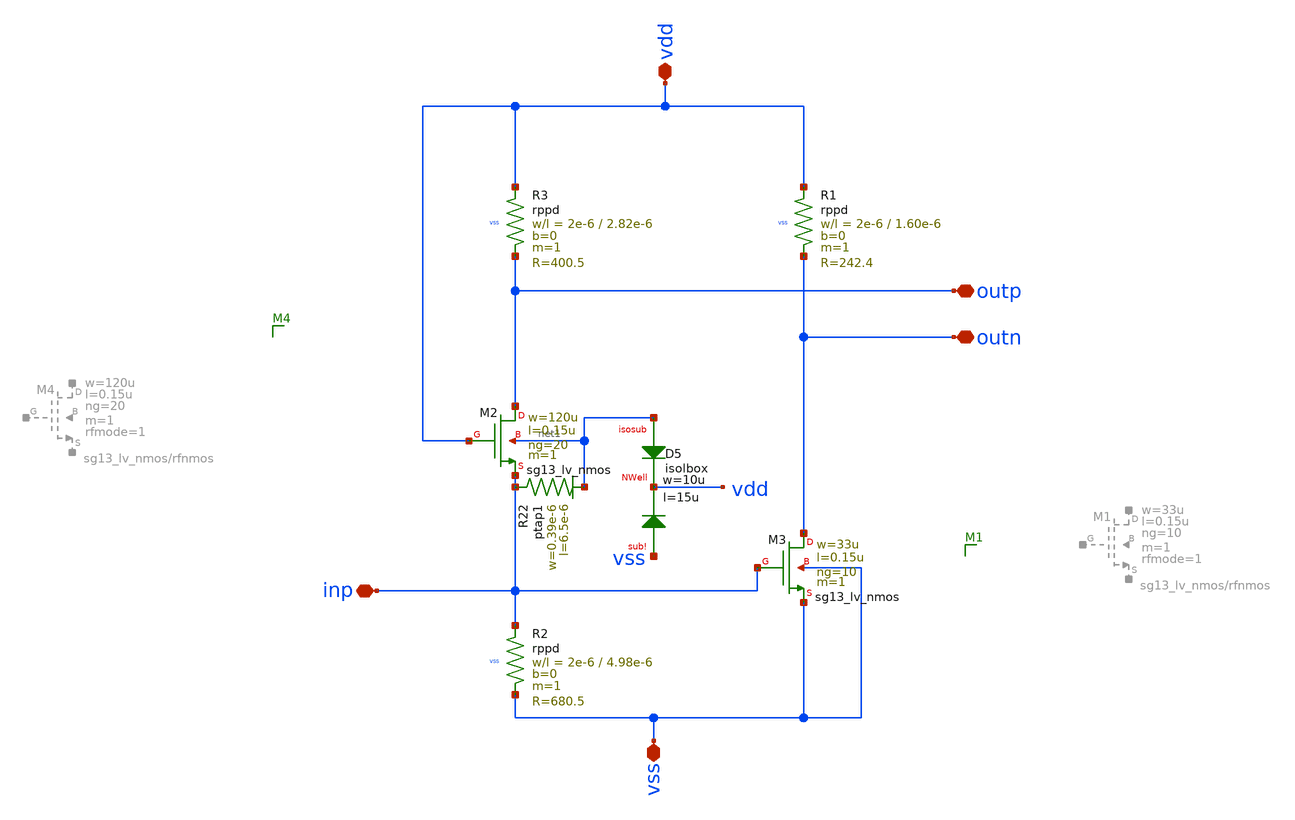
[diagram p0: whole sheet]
** sch_path: LNA7096-main/schematic/xschem/02_s2d/s2d.sch
**.subckt s2d vdd vss outp outn inp
*.iopin vdd
*.iopin vss
*.iopin outp
*.iopin outn
*.iopin inp
XR3 vdd outp vss rppd w=2e-6 l=2.82e-6 m=1 b=0 mm_ok=1
XR1 vdd outn vss rppd w=2e-6 l=1.60e-6 m=1 b=0 mm_ok=1
XR2 inp vss vss rppd w=2e-6 l=4.98e-6 m=1 b=0 mm_ok=1
XM2 outp vdd inp net1 sg13_lv_nmos w=120u l=0.15u ng=20 m=1 mm_ok=1
XM3 outn inp vss vss sg13_lv_nmos w=33u l=0.15u ng=10 m=1 mm_ok=1
XD5 net1 vdd vss isolbox l=15u w=10u
XR22 inp net1 ptap1 R=60.07 w=0.39e-6 l=6.5e-6
**.ends
.end
